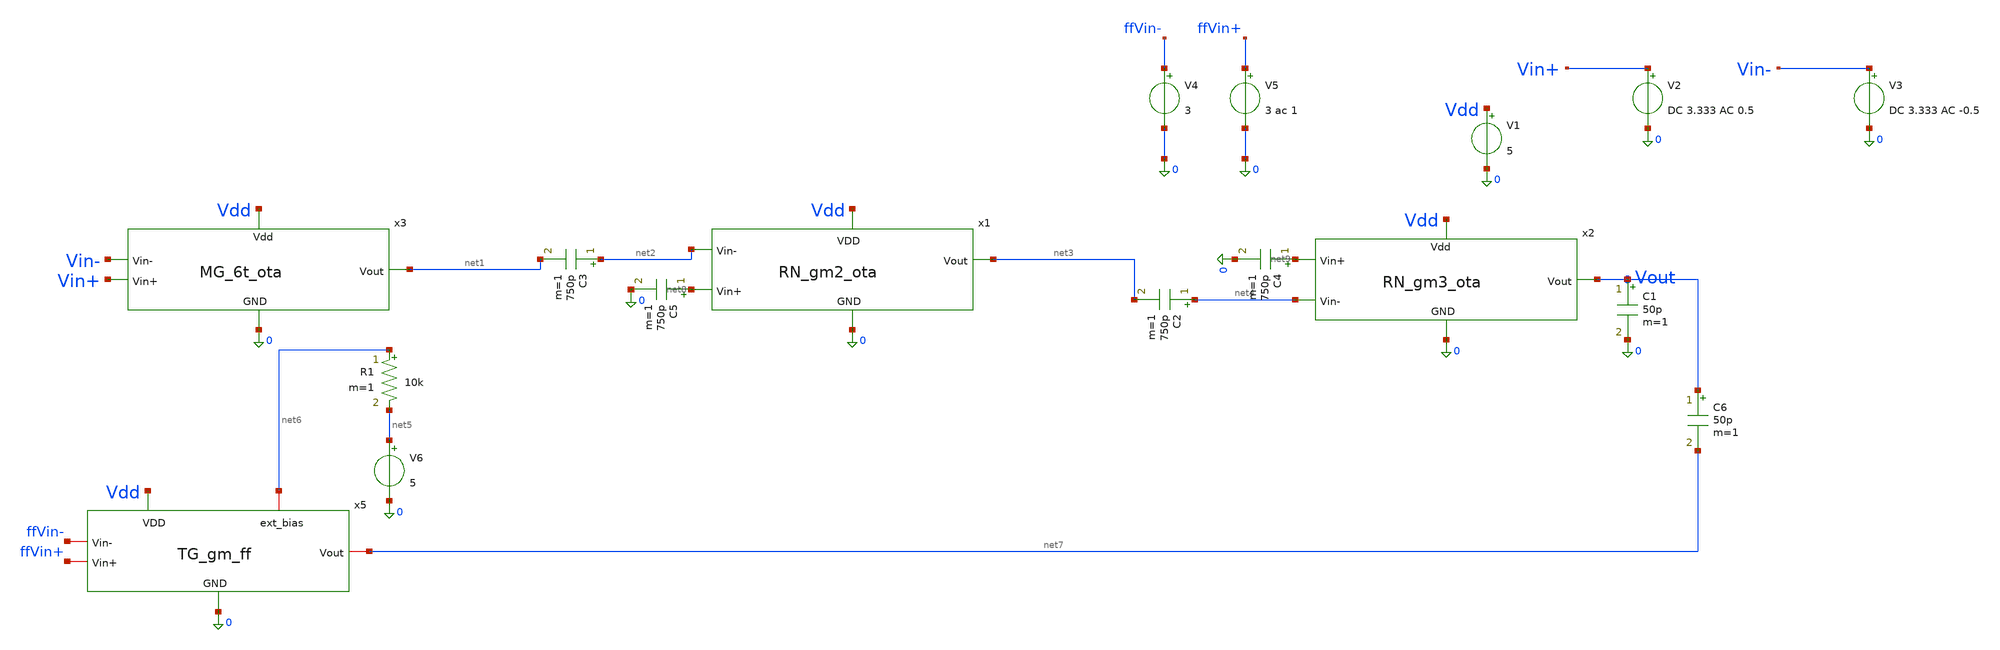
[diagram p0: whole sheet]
** sch_path: MRTMOS_chip_final/MRTMOS_chip_final_fraunhofer.sch
**.subckt MRTMOS_chip_final_fraunhofer
C1 Vout 0 50p m=1
V1 Vdd 0 5
V2 Vin+ 0 DC 3.333 AC 0.5
V3 Vin- 0 DC 3.333 AC -0.5
x1 Vdd net3 net2 net8 0 RN_gm2_ota
x2 Vdd Vout net9 net4 0 RN_gm3_ota
x3 Vdd net1 Vin- Vin+ 0 MG_6t_ota
C2 net4 net3 750p m=1
C3 net2 net1 750p m=1
V4 ffVin- 0 3
V5 ffVin+ 0 3 ac 1
R1 net6 net5 10k m=1
V6 net5 0 5
C4 net9 0 750p m=1
C5 net8 0 750p m=1
C6 Vout net7 50p m=1
x5 Vdd net7 ffVin- ffVin+ net6 0 TG_gm_ff
**** begin user architecture code


.include /foss/pdks/gf180mcuD/libs.tech/ngspice/design.ngspice
.lib /foss/pdks/gf180mcuD/libs.tech/ngspice/sm141064.ngspice typical
.lib /foss/pdks/gf180mcuD/libs.tech/ngspice/sm141064.ngspice res_typical
.lib /foss/pdks/gf180mcuD/libs.tech/ngspice/sm141064.ngspice moscap_typical
.lib /foss/pdks/gf180mcuD/libs.tech/ngspice/sm141064.ngspice mimcap_typical
.lib /foss/pdks/gf180mcuD/libs.tech/ngspice/sm141064.ngspice cap_mim




* AC & Transient Step Stimulus
* - DC bias: 3.0V
* - AC magnitude: 1V (for Bode plot)
* - Pulse: 2.95V to 3.05V step (100mV step), 5ns edges, 1MHz frequency (0.5us width, 1us period)


* --- 2. Simulation Control Block ---
.control
  save all

  * A. DC Operating Point Analysis
  op
  print v(Vout) v(Vin+) v(Vin-)

  * B. AC Sweep (Bode Plot: Gain & Phase)
  ac dec 20 1 100Meg
  set units = degrees
  plot vdb(Vout) vs frequency title 'Open-Loop AC Gain (dB)'
  plot cph(Vout) vs frequency title 'Open-Loop AC Phase (Degrees)'

  * C. Transient Analysis (1 MHz Step Response)
  * Run for 5 microseconds (5 complete 1MHz cycles) with a 1ns step
*  alter @v2[pulse] = [ 2.9 3.1 0 5n 5n 0.495u 1u ]
*  tran 1n 5u
*  plot v(Vin+) v(Vin-) v(Vout) title '1MHz Transient Step Response'

  * Save the raw data
  write RN_finaltb_sim.raw
.endc

.options savecurrents


**** end user architecture code
**.ends
.end
